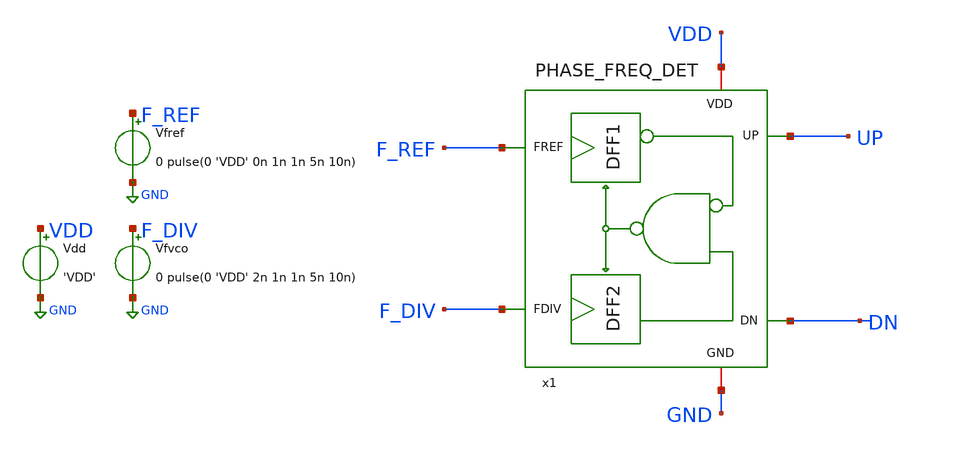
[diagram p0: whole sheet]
** sch_path: xschem/phase-freq-detector/tb_PHASE_FREQ_DET_PEX.sch
**.subckt tb_PHASE_FREQ_DET_PEX
Vdd VDD GND 'VDD'
Vfvco F_DIV GND 0 pulse(0 'VDD' 2n 1n 1n 5n 10n)
Vfref F_REF GND 0 pulse(0 'VDD' 0n 1n 1n 5n 10n)
x1 F_REF UP VDD GND F_DIV DN PHASE_FREQ_DET_PEX
**** begin user architecture code



.lib cornerMOSlv.lib mos_tt
.lib cornerMOShv.lib mos_tt
.lib cornerHBT.lib hbt_typ
.lib cornerRES.lib res_typ
.include /foss/pdks/ihp-sg13g2/libs.ref/sg13g2_stdcell/spice/sg13g2_stdcell.spice
.global VDD GND







.param RAW_TEMP = agauss(40, 30, 1)
.param TEMPGAUSS = max(20, min(RAW_TEMP, 80))
.option temp = 'TEMPGAUSS'
.param VDDGAUSS = agauss(1.2, 0.05, 1)
.include /foss/designs/unicasss-tools/SG13G2_2.4GHz_LC_VCO_FPLL/pex/PHASE_FREQ_DET__PHASE_FREQ_DET/magic_RC/PHASE_FREQ_DET.pex.spice
.param VDD = 'VDDGAUSS'
* analysis

.tran 100p 30n uic

.control
let i = 0
dowhile i < 10
  reset
  run
  write tb_PHASE_FREQ_DET_PEX.raw
  set appendwrite
  reset
  let i = i + 1
end
quit
.endc



**** end user architecture code
**.ends
.GLOBAL GND
.end
